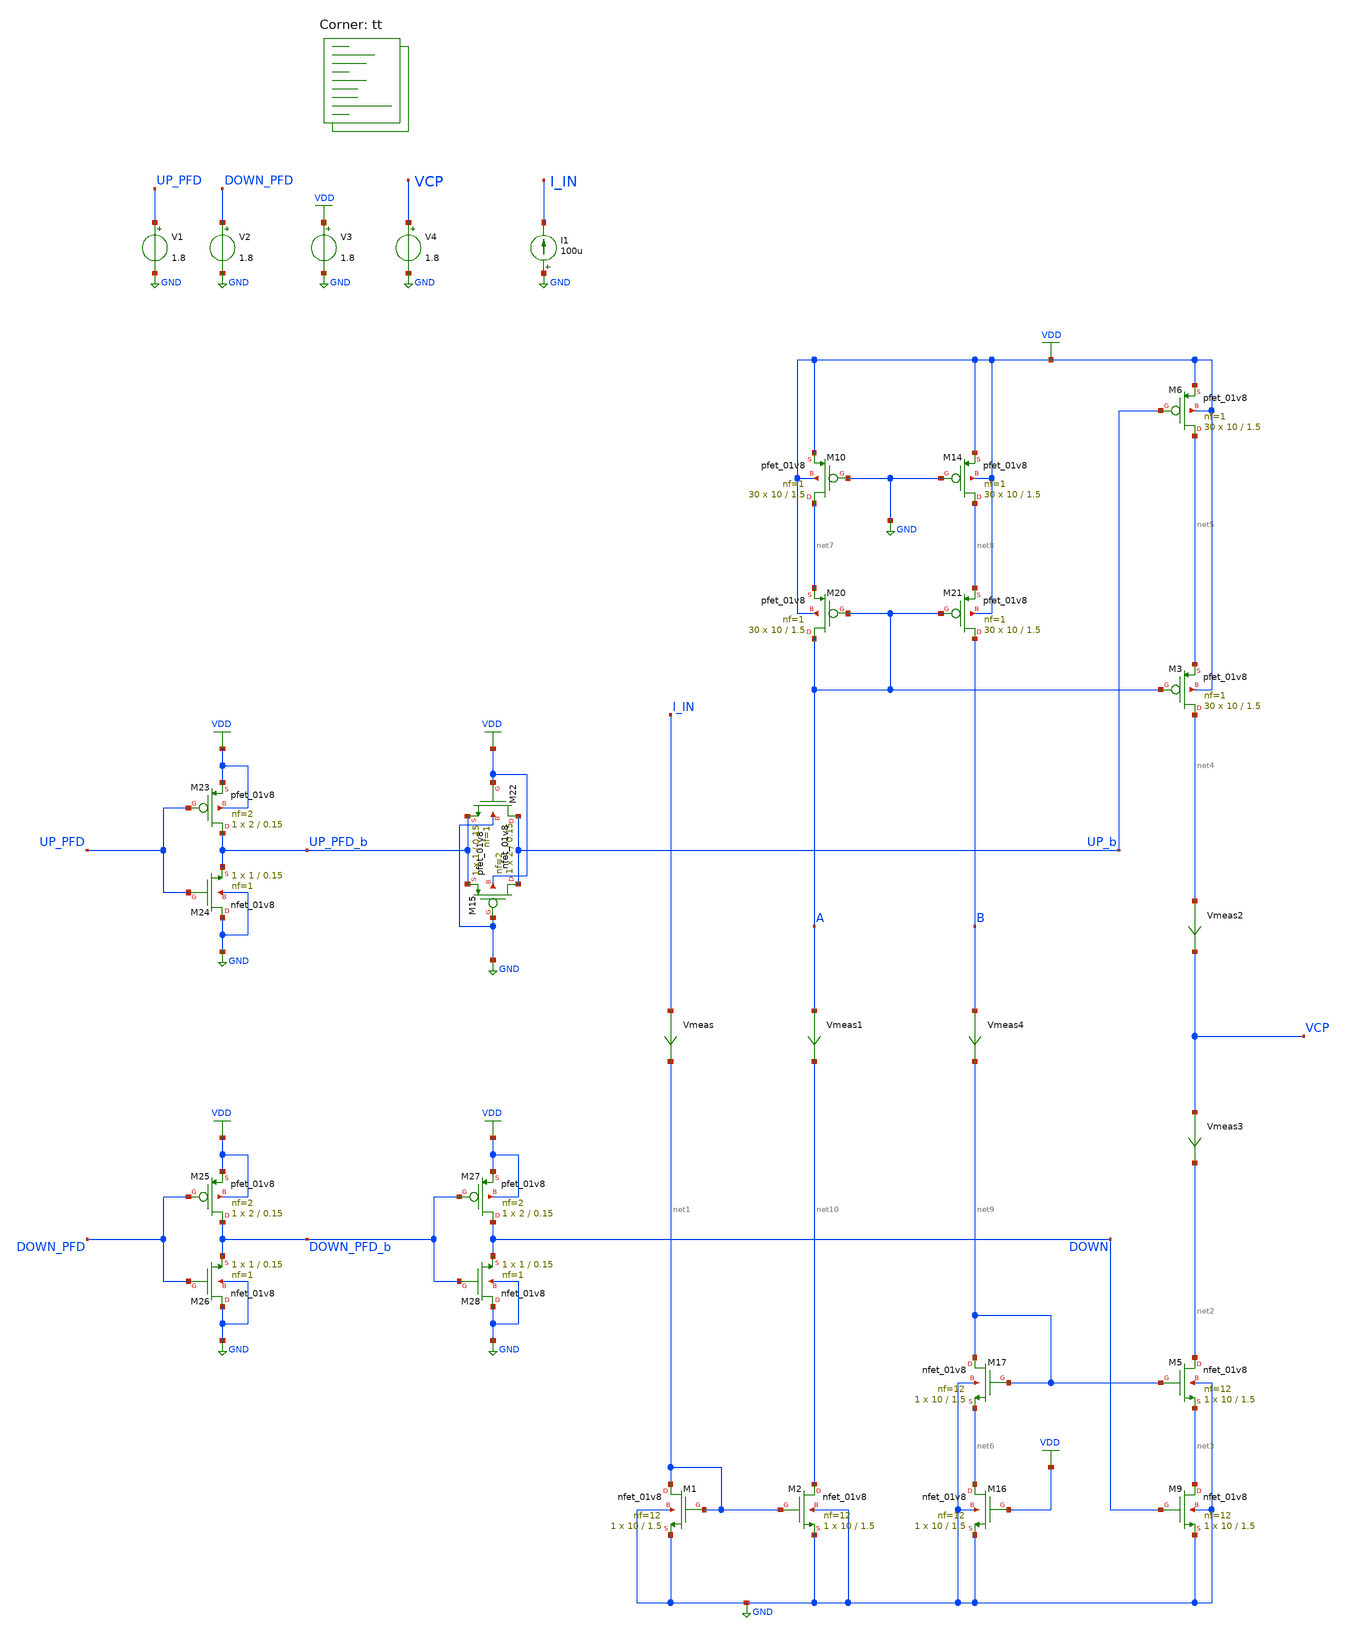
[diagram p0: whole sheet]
** sch_path: projects/pll/charge_pump/xschem_ngspice/charge_pump_DC3.sch
**.subckt charge_pump_DC3
XM1 net1 net1 GND GND sky130_fd_pr__nfet_01v8 L=1.5 W=10 nf=12 ad='int((nf+1)/2) * W/nf * 0.29' as='int((nf+2)/2) * W/nf * 0.29'
+ pd='2*int((nf+1)/2) * (W/nf + 0.29)' ps='2*int((nf+2)/2) * (W/nf + 0.29)' nrd='0.29 / W' nrs='0.29 / W'
+ sa=0 sb=0 sd=0 mult=1 m=1
XM2 net10 net1 GND GND sky130_fd_pr__nfet_01v8 L=1.5 W=10 nf=12 ad='int((nf+1)/2) * W/nf * 0.29' as='int((nf+2)/2) * W/nf * 0.29'
+ pd='2*int((nf+1)/2) * (W/nf + 0.29)' ps='2*int((nf+2)/2) * (W/nf + 0.29)' nrd='0.29 / W' nrs='0.29 / W'
+ sa=0 sb=0 sd=0 mult=1 m=1
Vmeas I_IN net1 0
.save i(vmeas)
XM6 net5 UP_b VDD VDD sky130_fd_pr__pfet_01v8 L=1.5 W=10 nf=1 ad='int((nf+1)/2) * W/nf * 0.29' as='int((nf+2)/2) * W/nf * 0.29'
+ pd='2*int((nf+1)/2) * (W/nf + 0.29)' ps='2*int((nf+2)/2) * (W/nf + 0.29)' nrd='0.29 / W' nrs='0.29 / W'
+ sa=0 sb=0 sd=0 mult=30 m=30
Vmeas2 net4 VCP 0
.save i(vmeas2)
Vmeas3 VCP net2 0
.save i(vmeas3)
XM9 net3 DOWN GND GND sky130_fd_pr__nfet_01v8 L=1.5 W=10 nf=12 ad='int((nf+1)/2) * W/nf * 0.29' as='int((nf+2)/2) * W/nf * 0.29'
+ pd='2*int((nf+1)/2) * (W/nf + 0.29)' ps='2*int((nf+2)/2) * (W/nf + 0.29)' nrd='0.29 / W' nrs='0.29 / W'
+ sa=0 sb=0 sd=0 mult=1 m=1
XM3 net4 A net5 VDD sky130_fd_pr__pfet_01v8 L=1.5 W=10 nf=1 ad='int((nf+1)/2) * W/nf * 0.29' as='int((nf+2)/2) * W/nf * 0.29'
+ pd='2*int((nf+1)/2) * (W/nf + 0.29)' ps='2*int((nf+2)/2) * (W/nf + 0.29)' nrd='0.29 / W' nrs='0.29 / W'
+ sa=0 sb=0 sd=0 mult=30 m=30
XM5 net2 net9 net3 GND sky130_fd_pr__nfet_01v8 L=1.5 W=10 nf=12 ad='int((nf+1)/2) * W/nf * 0.29' as='int((nf+2)/2) * W/nf * 0.29'
+ pd='2*int((nf+1)/2) * (W/nf + 0.29)' ps='2*int((nf+2)/2) * (W/nf + 0.29)' nrd='0.29 / W' nrs='0.29 / W'
+ sa=0 sb=0 sd=0 mult=1 m=1
XM10 net7 GND VDD VDD sky130_fd_pr__pfet_01v8 L=1.5 W=10 nf=1 ad='int((nf+1)/2) * W/nf * 0.29' as='int((nf+2)/2) * W/nf * 0.29'
+ pd='2*int((nf+1)/2) * (W/nf + 0.29)' ps='2*int((nf+2)/2) * (W/nf + 0.29)' nrd='0.29 / W' nrs='0.29 / W'
+ sa=0 sb=0 sd=0 mult=30 m=30
XM14 net8 GND VDD VDD sky130_fd_pr__pfet_01v8 L=1.5 W=10 nf=1 ad='int((nf+1)/2) * W/nf * 0.29' as='int((nf+2)/2) * W/nf * 0.29'
+ pd='2*int((nf+1)/2) * (W/nf + 0.29)' ps='2*int((nf+2)/2) * (W/nf + 0.29)' nrd='0.29 / W' nrs='0.29 / W'
+ sa=0 sb=0 sd=0 mult=30 m=30
XM16 net6 VDD GND GND sky130_fd_pr__nfet_01v8 L=1.5 W=10 nf=12 ad='int((nf+1)/2) * W/nf * 0.29' as='int((nf+2)/2) * W/nf * 0.29'
+ pd='2*int((nf+1)/2) * (W/nf + 0.29)' ps='2*int((nf+2)/2) * (W/nf + 0.29)' nrd='0.29 / W' nrs='0.29 / W'
+ sa=0 sb=0 sd=0 mult=1 m=1
XM17 net9 net9 net6 GND sky130_fd_pr__nfet_01v8 L=1.5 W=10 nf=12 ad='int((nf+1)/2) * W/nf * 0.29' as='int((nf+2)/2) * W/nf * 0.29'
+ pd='2*int((nf+1)/2) * (W/nf + 0.29)' ps='2*int((nf+2)/2) * (W/nf + 0.29)' nrd='0.29 / W' nrs='0.29 / W'
+ sa=0 sb=0 sd=0 mult=1 m=1
XM20 A A net7 VDD sky130_fd_pr__pfet_01v8 L=1.5 W=10 nf=1 ad='int((nf+1)/2) * W/nf * 0.29' as='int((nf+2)/2) * W/nf * 0.29'
+ pd='2*int((nf+1)/2) * (W/nf + 0.29)' ps='2*int((nf+2)/2) * (W/nf + 0.29)' nrd='0.29 / W' nrs='0.29 / W'
+ sa=0 sb=0 sd=0 mult=30 m=30
XM21 B A net8 VDD sky130_fd_pr__pfet_01v8 L=1.5 W=10 nf=1 ad='int((nf+1)/2) * W/nf * 0.29' as='int((nf+2)/2) * W/nf * 0.29'
+ pd='2*int((nf+1)/2) * (W/nf + 0.29)' ps='2*int((nf+2)/2) * (W/nf + 0.29)' nrd='0.29 / W' nrs='0.29 / W'
+ sa=0 sb=0 sd=0 mult=30 m=30
Vmeas1 A net10 0
.save i(vmeas1)
Vmeas4 B net9 0
.save i(vmeas4)
XM15 UP_b GND UP_PFD_b VDD sky130_fd_pr__pfet_01v8 L=0.15 W=2 nf=2 ad='int((nf+1)/2) * W/nf * 0.29' as='int((nf+2)/2) * W/nf * 0.29'
+ pd='2*int((nf+1)/2) * (W/nf + 0.29)' ps='2*int((nf+2)/2) * (W/nf + 0.29)' nrd='0.29 / W' nrs='0.29 / W'
+ sa=0 sb=0 sd=0 mult=1 m=1
XM22 UP_b VDD UP_PFD_b GND sky130_fd_pr__nfet_01v8 L=0.15 W=1 nf=1 ad='int((nf+1)/2) * W/nf * 0.29' as='int((nf+2)/2) * W/nf * 0.29'
+ pd='2*int((nf+1)/2) * (W/nf + 0.29)' ps='2*int((nf+2)/2) * (W/nf + 0.29)' nrd='0.29 / W' nrs='0.29 / W'
+ sa=0 sb=0 sd=0 mult=1 m=1
XM23 UP_PFD_b UP_PFD VDD VDD sky130_fd_pr__pfet_01v8 L=0.15 W=2 nf=2 ad='int((nf+1)/2) * W/nf * 0.29'
+ as='int((nf+2)/2) * W/nf * 0.29' pd='2*int((nf+1)/2) * (W/nf + 0.29)' ps='2*int((nf+2)/2) * (W/nf + 0.29)'
+ nrd='0.29 / W' nrs='0.29 / W' sa=0 sb=0 sd=0 mult=1 m=1
XM24 GND UP_PFD UP_PFD_b GND sky130_fd_pr__nfet_01v8 L=0.15 W=1 nf=1 ad='int((nf+1)/2) * W/nf * 0.29'
+ as='int((nf+2)/2) * W/nf * 0.29' pd='2*int((nf+1)/2) * (W/nf + 0.29)' ps='2*int((nf+2)/2) * (W/nf + 0.29)'
+ nrd='0.29 / W' nrs='0.29 / W' sa=0 sb=0 sd=0 mult=1 m=1
XM25 DOWN_PFD_b DOWN_PFD VDD VDD sky130_fd_pr__pfet_01v8 L=0.15 W=2 nf=2 ad='int((nf+1)/2) * W/nf * 0.29'
+ as='int((nf+2)/2) * W/nf * 0.29' pd='2*int((nf+1)/2) * (W/nf + 0.29)' ps='2*int((nf+2)/2) * (W/nf + 0.29)'
+ nrd='0.29 / W' nrs='0.29 / W' sa=0 sb=0 sd=0 mult=1 m=1
XM26 GND DOWN_PFD DOWN_PFD_b GND sky130_fd_pr__nfet_01v8 L=0.15 W=1 nf=1 ad='int((nf+1)/2) * W/nf * 0.29'
+ as='int((nf+2)/2) * W/nf * 0.29' pd='2*int((nf+1)/2) * (W/nf + 0.29)' ps='2*int((nf+2)/2) * (W/nf + 0.29)'
+ nrd='0.29 / W' nrs='0.29 / W' sa=0 sb=0 sd=0 mult=1 m=1
XM27 DOWN DOWN_PFD_b VDD VDD sky130_fd_pr__pfet_01v8 L=0.15 W=2 nf=2 ad='int((nf+1)/2) * W/nf * 0.29'
+ as='int((nf+2)/2) * W/nf * 0.29' pd='2*int((nf+1)/2) * (W/nf + 0.29)' ps='2*int((nf+2)/2) * (W/nf + 0.29)'
+ nrd='0.29 / W' nrs='0.29 / W' sa=0 sb=0 sd=0 mult=1 m=1
XM28 GND DOWN_PFD_b DOWN GND sky130_fd_pr__nfet_01v8 L=0.15 W=1 nf=1 ad='int((nf+1)/2) * W/nf * 0.29'
+ as='int((nf+2)/2) * W/nf * 0.29' pd='2*int((nf+1)/2) * (W/nf + 0.29)' ps='2*int((nf+2)/2) * (W/nf + 0.29)'
+ nrd='0.29 / W' nrs='0.29 / W' sa=0 sb=0 sd=0 mult=1 m=1
V3 VDD GND 1.8
I1 GND I_IN 100u
V1 UP_PFD GND 1.8
V2 DOWN_PFD GND 1.8
V4 VCP GND 1.8
**** begin user architecture code
.lib $::SKYWATER_MODELS/sky130.lib.spice tt



.include /foss/pdks/sky130A/libs.ref/sky130_fd_sc_hd/spice/sky130_fd_sc_hd.spice

.option method=gear trtol1
.option wnflag=1
.option savecurrents

* .temp = 75

* .ic v(vout) = 0

.control
  * save v(up_pfd) v(down_pfd) v(up_pfd_b) v(down_pfd_b) v(up) v(up_b) v(down) v(down_b) v(x)
+ v(vout) v(up_input) v(down_input)
  save all

  * tran 1ns 10us
  dc v4 0 1.8 0.01 v1 0 1.8 1.8
  remzerovec
  write charge_pump_DC3.raw
  * wrdata /foss/designs/my_design/projects/pll/pfd/xschem_ngspice/charge_pump3_QA.txt v(osc)
  set appendwrite

.endc






**** end user architecture code
**.ends
.GLOBAL GND
.GLOBAL VDD
.end
